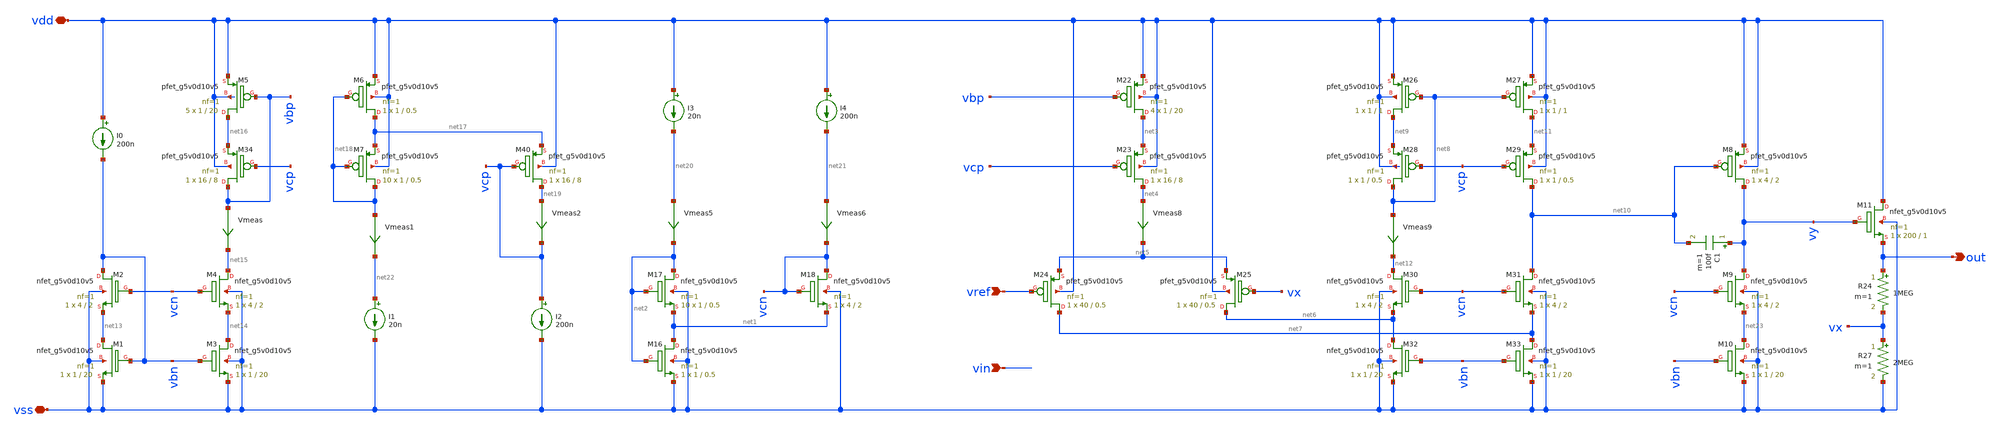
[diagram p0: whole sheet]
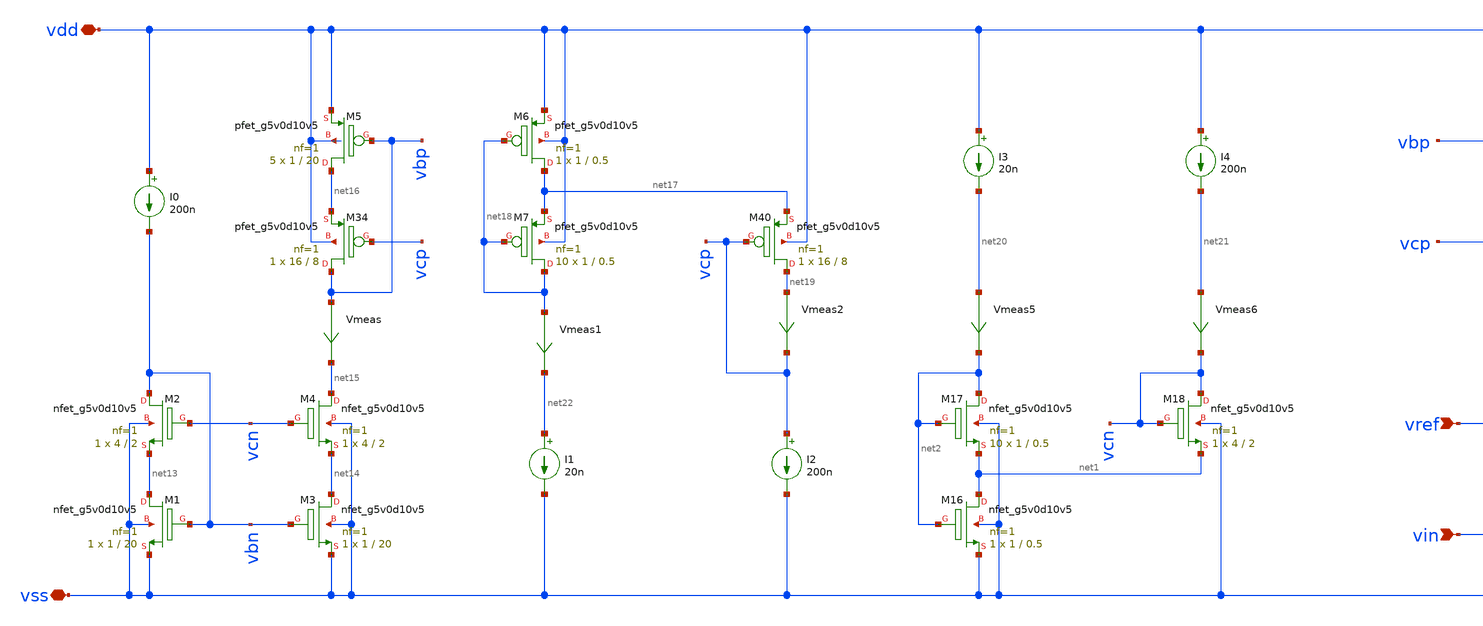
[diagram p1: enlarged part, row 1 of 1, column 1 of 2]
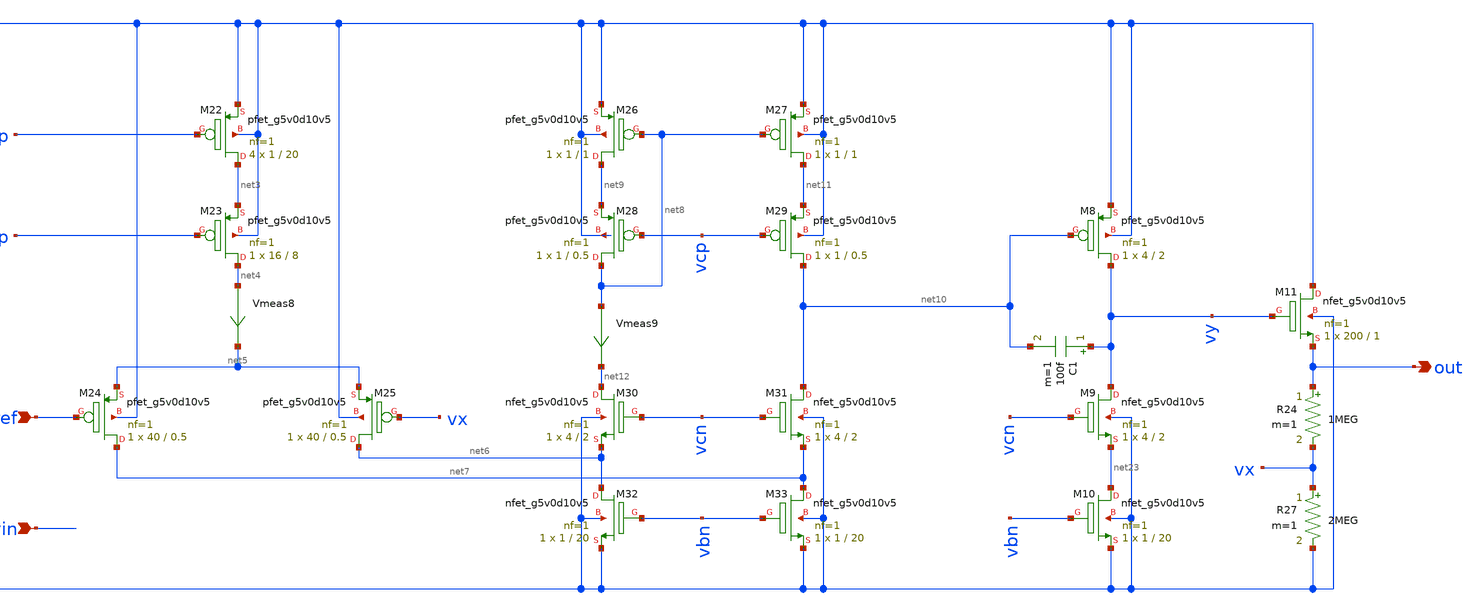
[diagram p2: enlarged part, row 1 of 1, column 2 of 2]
** sch_path: xschem/ldo.sch
**.subckt ldo out vref vdd vss vin
*.opin out
*.ipin vref
*.iopin vdd
*.iopin vss
*.ipin vin
XM1 net13 vbn vss vss sky130_fd_pr__nfet_g5v0d10v5 L=20 W=1 nf=1 ad='int((nf+1)/2) * W/nf * 0.29' as='int((nf+2)/2) * W/nf * 0.29'
+ pd='2*int((nf+1)/2) * (W/nf + 0.29)' ps='2*int((nf+2)/2) * (W/nf + 0.29)' nrd='0.29 / W' nrs='0.29 / W'
+ sa=0 sb=0 sd=0 mult=1 m=1
XM3 net14 vbn vss vss sky130_fd_pr__nfet_g5v0d10v5 L=20 W=1 nf=1 ad='int((nf+1)/2) * W/nf * 0.29' as='int((nf+2)/2) * W/nf * 0.29'
+ pd='2*int((nf+1)/2) * (W/nf + 0.29)' ps='2*int((nf+2)/2) * (W/nf + 0.29)' nrd='0.29 / W' nrs='0.29 / W'
+ sa=0 sb=0 sd=0 mult=1 m=1
XM5 net16 vbp vdd vdd sky130_fd_pr__pfet_g5v0d10v5 L=20 W=1 nf=1 ad='int((nf+1)/2) * W/nf * 0.29' as='int((nf+2)/2) * W/nf * 0.29'
+ pd='2*int((nf+1)/2) * (W/nf + 0.29)' ps='2*int((nf+2)/2) * (W/nf + 0.29)' nrd='0.29 / W' nrs='0.29 / W'
+ sa=0 sb=0 sd=0 mult=5 m=5
I0 vdd vbn 200n
XM16 net1 net2 vss vss sky130_fd_pr__nfet_g5v0d10v5 L=0.5 W=1 nf=1 ad='int((nf+1)/2) * W/nf * 0.29' as='int((nf+2)/2) * W/nf * 0.29'
+ pd='2*int((nf+1)/2) * (W/nf + 0.29)' ps='2*int((nf+2)/2) * (W/nf + 0.29)' nrd='0.29 / W' nrs='0.29 / W'
+ sa=0 sb=0 sd=0 mult=1 m=1
XM17 net2 net2 net1 vss sky130_fd_pr__nfet_g5v0d10v5 L=0.5 W=1 nf=1 ad='int((nf+1)/2) * W/nf * 0.29'
+ as='int((nf+2)/2) * W/nf * 0.29' pd='2*int((nf+1)/2) * (W/nf + 0.29)' ps='2*int((nf+2)/2) * (W/nf + 0.29)'
+ nrd='0.29 / W' nrs='0.29 / W' sa=0 sb=0 sd=0 mult=10 m=10
XM18 vcn vcn net1 vss sky130_fd_pr__nfet_g5v0d10v5 L=2 W=4 nf=1 ad='int((nf+1)/2) * W/nf * 0.29' as='int((nf+2)/2) * W/nf * 0.29'
+ pd='2*int((nf+1)/2) * (W/nf + 0.29)' ps='2*int((nf+2)/2) * (W/nf + 0.29)' nrd='0.29 / W' nrs='0.29 / W'
+ sa=0 sb=0 sd=0 mult=1 m=1
Vmeas vbp net15 0
.save i(vmeas)
Vmeas5 net20 net2 0
.save i(vmeas5)
Vmeas6 net21 vcn 0
.save i(vmeas6)
XM22 net3 vbp vdd vdd sky130_fd_pr__pfet_g5v0d10v5 L=20 W=1 nf=1 ad='int((nf+1)/2) * W/nf * 0.29' as='int((nf+2)/2) * W/nf * 0.29'
+ pd='2*int((nf+1)/2) * (W/nf + 0.29)' ps='2*int((nf+2)/2) * (W/nf + 0.29)' nrd='0.29 / W' nrs='0.29 / W'
+ sa=0 sb=0 sd=0 mult=4 m=4
XM23 net4 vcp net3 vdd sky130_fd_pr__pfet_g5v0d10v5 L=8 W=16 nf=1 ad='int((nf+1)/2) * W/nf * 0.29' as='int((nf+2)/2) * W/nf * 0.29'
+ pd='2*int((nf+1)/2) * (W/nf + 0.29)' ps='2*int((nf+2)/2) * (W/nf + 0.29)' nrd='0.29 / W' nrs='0.29 / W'
+ sa=0 sb=0 sd=0 mult=1 m=1
Vmeas8 net4 net5 0
.save i(vmeas8)
XM24 net7 vref net5 vdd sky130_fd_pr__pfet_g5v0d10v5 L=0.5 W=40 nf=1 ad='int((nf+1)/2) * W/nf * 0.29'
+ as='int((nf+2)/2) * W/nf * 0.29' pd='2*int((nf+1)/2) * (W/nf + 0.29)' ps='2*int((nf+2)/2) * (W/nf + 0.29)'
+ nrd='0.29 / W' nrs='0.29 / W' sa=0 sb=0 sd=0 mult=1 m=1
XM25 net6 vx net5 vdd sky130_fd_pr__pfet_g5v0d10v5 L=0.5 W=40 nf=1 ad='int((nf+1)/2) * W/nf * 0.29' as='int((nf+2)/2) * W/nf * 0.29'
+ pd='2*int((nf+1)/2) * (W/nf + 0.29)' ps='2*int((nf+2)/2) * (W/nf + 0.29)' nrd='0.29 / W' nrs='0.29 / W'
+ sa=0 sb=0 sd=0 mult=1 m=1
XM26 net9 net8 vdd vdd sky130_fd_pr__pfet_g5v0d10v5 L=1 W=1 nf=1 ad='int((nf+1)/2) * W/nf * 0.29' as='int((nf+2)/2) * W/nf * 0.29'
+ pd='2*int((nf+1)/2) * (W/nf + 0.29)' ps='2*int((nf+2)/2) * (W/nf + 0.29)' nrd='0.29 / W' nrs='0.29 / W'
+ sa=0 sb=0 sd=0 mult=1 m=1
XM27 net11 net8 vdd vdd sky130_fd_pr__pfet_g5v0d10v5 L=1 W=1 nf=1 ad='int((nf+1)/2) * W/nf * 0.29' as='int((nf+2)/2) * W/nf * 0.29'
+ pd='2*int((nf+1)/2) * (W/nf + 0.29)' ps='2*int((nf+2)/2) * (W/nf + 0.29)' nrd='0.29 / W' nrs='0.29 / W'
+ sa=0 sb=0 sd=0 mult=1 m=1
XM28 net8 vcp net9 vdd sky130_fd_pr__pfet_g5v0d10v5 L=0.5 W=1 nf=1 ad='int((nf+1)/2) * W/nf * 0.29' as='int((nf+2)/2) * W/nf * 0.29'
+ pd='2*int((nf+1)/2) * (W/nf + 0.29)' ps='2*int((nf+2)/2) * (W/nf + 0.29)' nrd='0.29 / W' nrs='0.29 / W'
+ sa=0 sb=0 sd=0 mult=1 m=1
XM29 net10 vcp net11 vdd sky130_fd_pr__pfet_g5v0d10v5 L=0.5 W=1 nf=1 ad='int((nf+1)/2) * W/nf * 0.29'
+ as='int((nf+2)/2) * W/nf * 0.29' pd='2*int((nf+1)/2) * (W/nf + 0.29)' ps='2*int((nf+2)/2) * (W/nf + 0.29)'
+ nrd='0.29 / W' nrs='0.29 / W' sa=0 sb=0 sd=0 mult=1 m=1
XM30 net12 vcn net6 vss sky130_fd_pr__nfet_g5v0d10v5 L=2 W=4 nf=1 ad='int((nf+1)/2) * W/nf * 0.29' as='int((nf+2)/2) * W/nf * 0.29'
+ pd='2*int((nf+1)/2) * (W/nf + 0.29)' ps='2*int((nf+2)/2) * (W/nf + 0.29)' nrd='0.29 / W' nrs='0.29 / W'
+ sa=0 sb=0 sd=0 mult=1 m=1
XM31 net10 vcn net7 vss sky130_fd_pr__nfet_g5v0d10v5 L=2 W=4 nf=1 ad='int((nf+1)/2) * W/nf * 0.29' as='int((nf+2)/2) * W/nf * 0.29'
+ pd='2*int((nf+1)/2) * (W/nf + 0.29)' ps='2*int((nf+2)/2) * (W/nf + 0.29)' nrd='0.29 / W' nrs='0.29 / W'
+ sa=0 sb=0 sd=0 mult=1 m=1
XM32 net6 vbn vss vss sky130_fd_pr__nfet_g5v0d10v5 L=20 W=1 nf=1 ad='int((nf+1)/2) * W/nf * 0.29' as='int((nf+2)/2) * W/nf * 0.29'
+ pd='2*int((nf+1)/2) * (W/nf + 0.29)' ps='2*int((nf+2)/2) * (W/nf + 0.29)' nrd='0.29 / W' nrs='0.29 / W'
+ sa=0 sb=0 sd=0 mult=1 m=1
XM33 net7 vbn vss vss sky130_fd_pr__nfet_g5v0d10v5 L=20 W=1 nf=1 ad='int((nf+1)/2) * W/nf * 0.29' as='int((nf+2)/2) * W/nf * 0.29'
+ pd='2*int((nf+1)/2) * (W/nf + 0.29)' ps='2*int((nf+2)/2) * (W/nf + 0.29)' nrd='0.29 / W' nrs='0.29 / W'
+ sa=0 sb=0 sd=0 mult=1 m=1
Vmeas9 net8 net12 0
.save i(vmeas9)
XM2 vbn vcn net13 vss sky130_fd_pr__nfet_g5v0d10v5 L=2 W=4 nf=1 ad='int((nf+1)/2) * W/nf * 0.29' as='int((nf+2)/2) * W/nf * 0.29'
+ pd='2*int((nf+1)/2) * (W/nf + 0.29)' ps='2*int((nf+2)/2) * (W/nf + 0.29)' nrd='0.29 / W' nrs='0.29 / W'
+ sa=0 sb=0 sd=0 mult=1 m=1
XM4 net15 vcn net14 vss sky130_fd_pr__nfet_g5v0d10v5 L=2 W=4 nf=1 ad='int((nf+1)/2) * W/nf * 0.29' as='int((nf+2)/2) * W/nf * 0.29'
+ pd='2*int((nf+1)/2) * (W/nf + 0.29)' ps='2*int((nf+2)/2) * (W/nf + 0.29)' nrd='0.29 / W' nrs='0.29 / W'
+ sa=0 sb=0 sd=0 mult=1 m=1
XM34 vbp vcp net16 vdd sky130_fd_pr__pfet_g5v0d10v5 L=8 W=16 nf=1 ad='int((nf+1)/2) * W/nf * 0.29' as='int((nf+2)/2) * W/nf * 0.29'
+ pd='2*int((nf+1)/2) * (W/nf + 0.29)' ps='2*int((nf+2)/2) * (W/nf + 0.29)' nrd='0.29 / W' nrs='0.29 / W'
+ sa=0 sb=0 sd=0 mult=1 m=1
XM6 net17 net18 vdd vdd sky130_fd_pr__pfet_g5v0d10v5 L=0.5 W=1 nf=1 ad='int((nf+1)/2) * W/nf * 0.29'
+ as='int((nf+2)/2) * W/nf * 0.29' pd='2*int((nf+1)/2) * (W/nf + 0.29)' ps='2*int((nf+2)/2) * (W/nf + 0.29)'
+ nrd='0.29 / W' nrs='0.29 / W' sa=0 sb=0 sd=0 mult=1 m=1
XM7 net18 net18 net17 vdd sky130_fd_pr__pfet_g5v0d10v5 L=0.5 W=1 nf=1 ad='int((nf+1)/2) * W/nf * 0.29'
+ as='int((nf+2)/2) * W/nf * 0.29' pd='2*int((nf+1)/2) * (W/nf + 0.29)' ps='2*int((nf+2)/2) * (W/nf + 0.29)'
+ nrd='0.29 / W' nrs='0.29 / W' sa=0 sb=0 sd=0 mult=10 m=10
Vmeas1 net18 net22 0
.save i(vmeas1)
XM40 net19 vcp net17 vdd sky130_fd_pr__pfet_g5v0d10v5 L=8 W=16 nf=1 ad='int((nf+1)/2) * W/nf * 0.29'
+ as='int((nf+2)/2) * W/nf * 0.29' pd='2*int((nf+1)/2) * (W/nf + 0.29)' ps='2*int((nf+2)/2) * (W/nf + 0.29)'
+ nrd='0.29 / W' nrs='0.29 / W' sa=0 sb=0 sd=0 mult=1 m=1
Vmeas2 net19 vcp 0
.save i(vmeas2)
I1 net22 vss 20n
I2 vcp vss 200n
I3 vdd net20 20n
I4 vdd net21 200n
XM8 vy net10 vdd vdd sky130_fd_pr__pfet_g5v0d10v5 L=2 W=4 nf=1 ad='int((nf+1)/2) * W/nf * 0.29' as='int((nf+2)/2) * W/nf * 0.29'
+ pd='2*int((nf+1)/2) * (W/nf + 0.29)' ps='2*int((nf+2)/2) * (W/nf + 0.29)' nrd='0.29 / W' nrs='0.29 / W'
+ sa=0 sb=0 sd=0 mult=1 m=1
XM9 vy vcn net23 vss sky130_fd_pr__nfet_g5v0d10v5 L=2 W=4 nf=1 ad='int((nf+1)/2) * W/nf * 0.29' as='int((nf+2)/2) * W/nf * 0.29'
+ pd='2*int((nf+1)/2) * (W/nf + 0.29)' ps='2*int((nf+2)/2) * (W/nf + 0.29)' nrd='0.29 / W' nrs='0.29 / W'
+ sa=0 sb=0 sd=0 mult=1 m=1
XM10 net23 vbn vss vss sky130_fd_pr__nfet_g5v0d10v5 L=20 W=1 nf=1 ad='int((nf+1)/2) * W/nf * 0.29' as='int((nf+2)/2) * W/nf * 0.29'
+ pd='2*int((nf+1)/2) * (W/nf + 0.29)' ps='2*int((nf+2)/2) * (W/nf + 0.29)' nrd='0.29 / W' nrs='0.29 / W'
+ sa=0 sb=0 sd=0 mult=1 m=1
XM11 vdd vy out vss sky130_fd_pr__nfet_g5v0d10v5 L=1 W=200 nf=1 ad='int((nf+1)/2) * W/nf * 0.29' as='int((nf+2)/2) * W/nf * 0.29'
+ pd='2*int((nf+1)/2) * (W/nf + 0.29)' ps='2*int((nf+2)/2) * (W/nf + 0.29)' nrd='0.29 / W' nrs='0.29 / W'
+ sa=0 sb=0 sd=0 mult=1 m=1
R24 out vx 1MEG m=1
R27 vx vss 2MEG m=1
C1 vy net10 100f m=1
**** begin user architecture code

vref vref 0 1.2
vss vss 0 0
vdd vdd 0 pwl(0 0 1u 0 2u 3.3 300u 3.3) dc 3.3 ac 1
* vdd vdd 0 3.3
* vin vin 0 1.2 ac 1
.option savecurrents
.control
save all
save @m.xm27.msky130_fd_pr__pfet_g5v0d10v5[gds]
op
write ldo.raw
set appendwrite
* quit
* === analysis ===
ac dec 10 10 10MEG
write lod.raw
set units=degrees
plot db(out)
plot ph(out)
tran 10n 300u
write bias_generator.raw
plot v(out)
.endc


.lib $::SKYWATER_MODELS/sky130.lib.spice tt
**** end user architecture code
**.ends
.end
